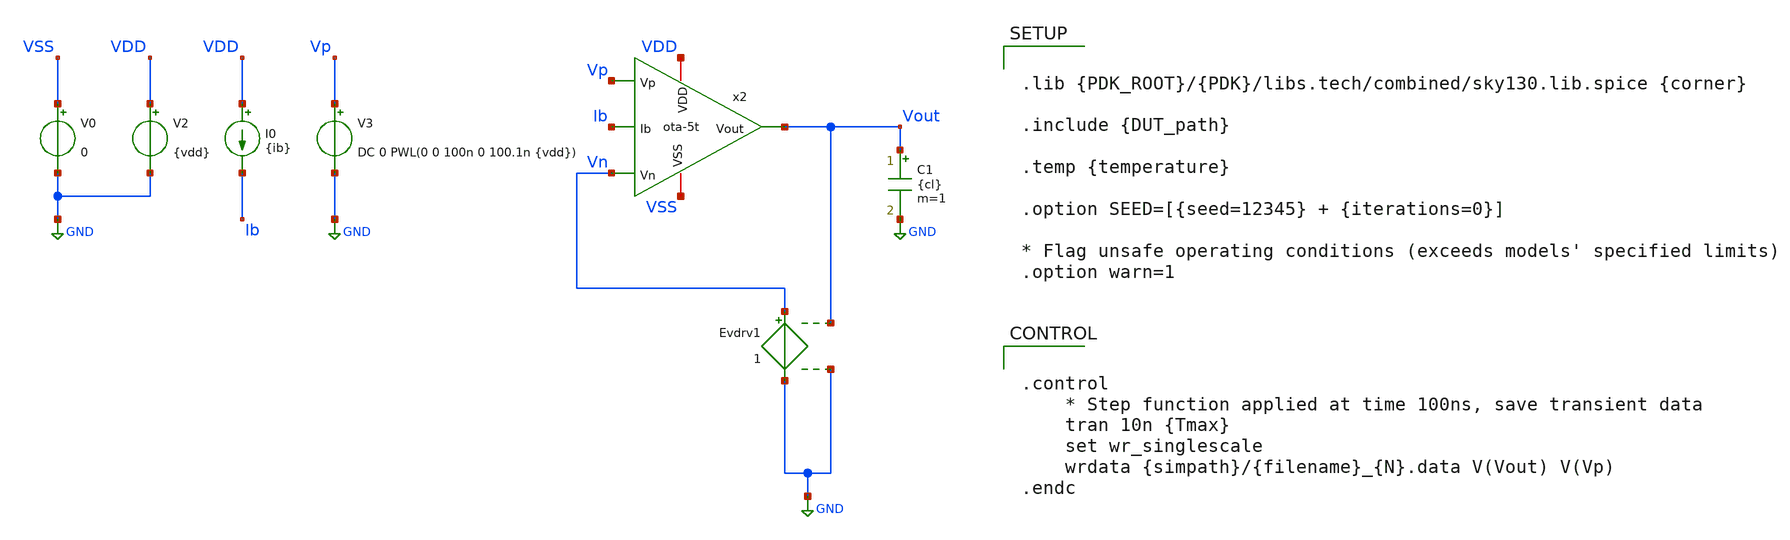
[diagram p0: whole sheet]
** sch_path: cace/templates/transient.sch
**.subckt transient
I0 VDD Ib {ib}
C1 Vout GND {cl} m=1
V0 VSS GND 0
V2 VDD GND {vdd}
x2 Vp Vn Vout VDD VSS Ib ota-5t
Evdrv1 Vn GND Vout GND 1
V3 Vp GND DC 0 PWL(0 0 100n 0 100.1n {vdd})
**** begin user architecture code


.control
    * Step function applied at time 100ns, save transient data
    tran 10n {Tmax}
    set wr_singlescale
    wrdata {simpath}/{filename}_{N}.data V(Vout) V(Vp)
.endc




.lib {PDK_ROOT}/{PDK}/libs.tech/combined/sky130.lib.spice {corner}

.include {DUT_path}

.temp {temperature}

.option SEED=[{seed=12345} + {iterations=0}]

* Flag unsafe operating conditions (exceeds models' specified limits)
.option warn=1


**** end user architecture code
**.ends
.GLOBAL GND
.end
